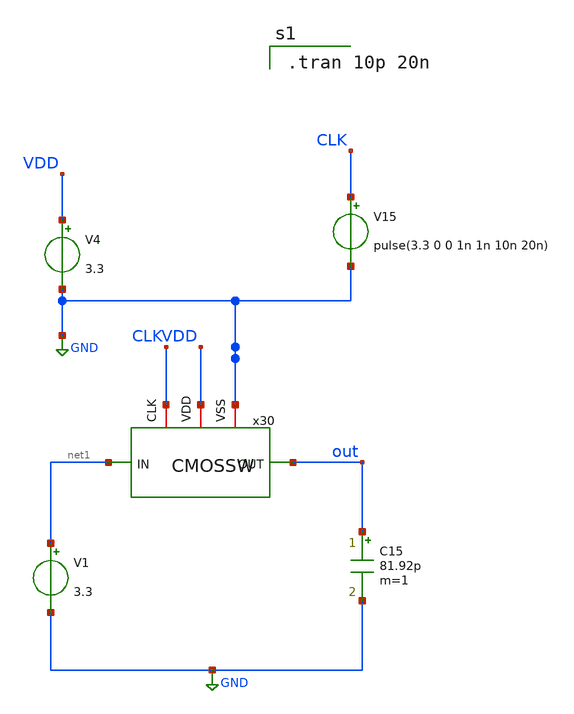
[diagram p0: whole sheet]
** sch_path: RC.sch
**.subckt RC
C15 out GND 81.92p m=1
x30 CLK GND out net1 VDD CMOSSW
V1 net1 GND 3.3
V4 VDD GND 3.3
V15 CLK GND pulse(3.3 0 0 1n 1n 10n 20n)
**** begin user architecture code

.tran 10p 20n

**** end user architecture code
**.ends

* expanding   symbol:  C:/Users/ISLab2/Documents/minimal_LR/CMOSSW.sym # of pins=5
** sym_path: CMOSSW.sym
** sch_path: CMOSSW.sch
.subckt CMOSSW CLK VSS OUT IN VDD
*.ipin IN
*.iopin VDD
*.iopin VSS
*.opin OUT
*.iopin CLK
M1 OUT CLK IN VSS nch w=10u l=0.35u as=0 ps=0 ad=0 pd=0 m=1
M2 OUT net1 IN VDD pch w=10u l=0.35u as=0 ps=0 ad=0 pd=0 m=1
**** begin user architecture code


.include C:/Users/ISLab2/Documents/minimal_LR/minimal.txt

**** end user architecture code
x1 VDD net1 CLK VSS INV
.ends


* expanding   symbol:  C:/Users/ISLab2/Documents/minimal_LR/INV.sym # of pins=4
** sym_path: INV.sym
** sch_path: INV.sch
.subckt INV VDD OUT IN VSS
*.opin OUT
*.ipin IN
*.iopin VDD
*.iopin VSS
M2 OUT IN VDD VDD pch w=10u l=0.35u as=0 ps=0 ad=0 pd=0 m=1
M1 OUT IN VSS VSS nch w=5u l=0.35u as=0 ps=0 ad=0 pd=0 m=1
.ends

.GLOBAL GND
.end
